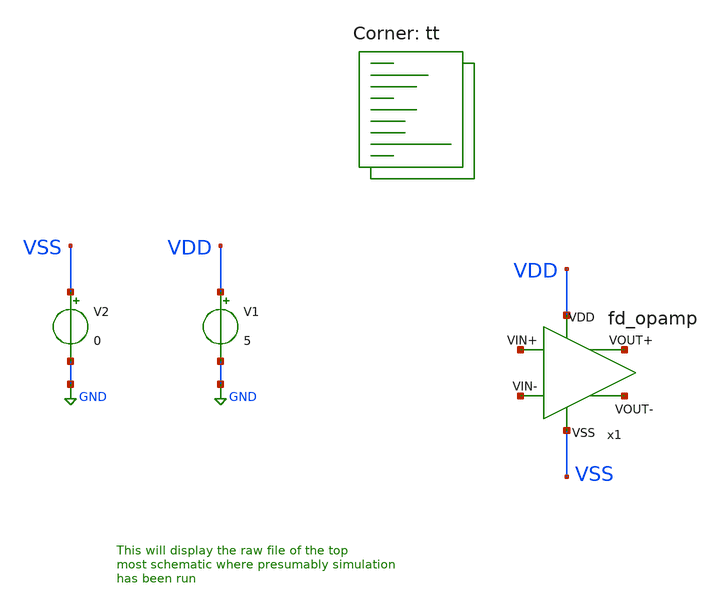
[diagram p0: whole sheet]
** sch_path: my_ip/sky130A/fully_differential_telescopic_cascode_5V_V1/tb/tb.sch
**.subckt tb
V1 VDD GND 5
V2 VSS GND 0
x1 VDD VSS net1 net2 net3 net4 fd_opamp
**** begin user architecture code
.lib $::SKYWATER_MODELS/sky130.lib.spice tt
**** end user architecture code
**.ends
.GLOBAL GND
**** begin user architecture code


* ngspice commands
.options savecurrents
.TEMP 27
.control
save all
save @m.x1.xm1.msky130_fd_pr__pfet_g5v0d10v5[gm]
save @m.x1.xm1.msky130_fd_pr__pfet_g5v0d10v5[vth]
save @m.x1.xm1.msky130_fd_pr__pfet_g5v0d10v5[vds]
save @m.x1.xm1.msky130_fd_pr__pfet_g5v0d10v5[vgs]

save @m.x1.xm2.msky130_fd_pr__pfet_g5v0d10v5[gm]
save @m.x1.xm2.msky130_fd_pr__pfet_g5v0d10v5[vth]
save @m.x1.xm2.msky130_fd_pr__pfet_g5v0d10v5[vds]
save @m.x1.xm2.msky130_fd_pr__pfet_g5v0d10v5[vgs]

save @m.x1.xm3.msky130_fd_pr__pfet_g5v0d10v5[gm]
save @m.x1.xm3.msky130_fd_pr__pfet_g5v0d10v5[vth]
save @m.x1.xm3.msky130_fd_pr__pfet_g5v0d10v5[vds]
save @m.x1.xm3.msky130_fd_pr__pfet_g5v0d10v5[vgs]

save @m.x1.xm4.msky130_fd_pr__pfet_g5v0d10v5[gm]
save @m.x1.xm4.msky130_fd_pr__pfet_g5v0d10v5[vth]
save @m.x1.xm4.msky130_fd_pr__pfet_g5v0d10v5[vds]
save @m.x1.xm4.msky130_fd_pr__pfet_g5v0d10v5[vgs]

save @m.x1.xm5.msky130_fd_pr__nfet_g5v0d10v5[gm]
save @m.x1.xm5.msky130_fd_pr__nfet_g5v0d10v5[vth]
save @m.x1.xm5.msky130_fd_pr__nfet_g5v0d10v5[vds]
save @m.x1.xm5.msky130_fd_pr__nfet_g5v0d10v5[vgs]

save @m.x1.xm6.msky130_fd_pr__nfet_g5v0d10v5[gm]
save @m.x1.xm6.msky130_fd_pr__nfet_g5v0d10v5[vth]
save @m.x1.xm6.msky130_fd_pr__nfet_g5v0d10v5[vds]
save @m.x1.xm6.msky130_fd_pr__nfet_g5v0d10v5[vgs]

save @m.x1.xm7.msky130_fd_pr__nfet_g5v0d10v5[gm]
save @m.x1.xm7.msky130_fd_pr__nfet_g5v0d10v5[vth]
save @m.x1.xm7.msky130_fd_pr__nfet_g5v0d10v5[vds]
save @m.x1.xm7.msky130_fd_pr__nfet_g5v0d10v5[vgs]

save @m.x1.xm8.msky130_fd_pr__nfet_g5v0d10v5[gm]
save @m.x1.xm8.msky130_fd_pr__nfet_g5v0d10v5[vth]
save @m.x1.xm8.msky130_fd_pr__nfet_g5v0d10v5[vds]
save @m.x1.xm8.msky130_fd_pr__nfet_g5v0d10v5[vgs]

op
write tb.raw

.endc



**** end user architecture code
.end
